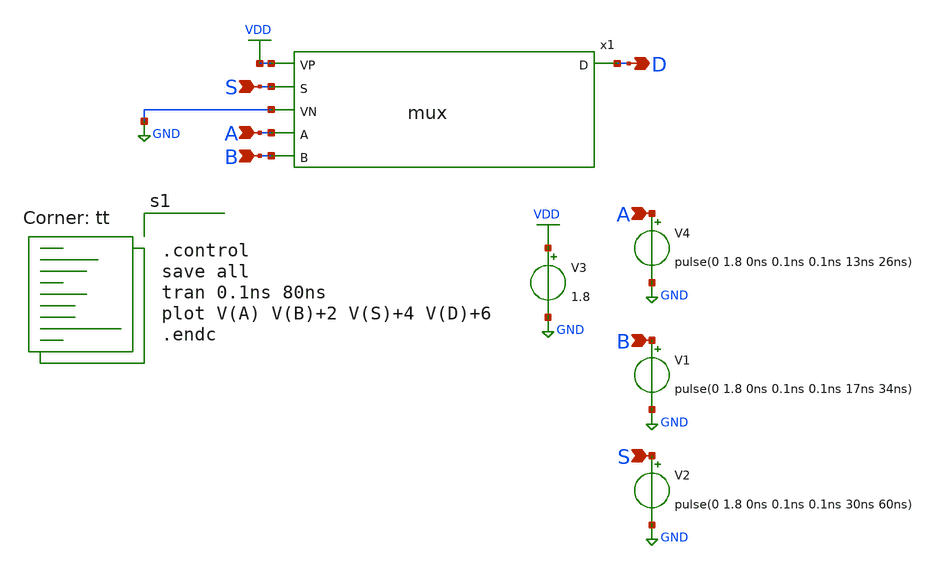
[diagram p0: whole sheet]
** sch_path: mux/xschem/tb_xschem_mux.sch
**.subckt tb_xschem_mux A B A B D S S
*.ipin A
*.ipin B
*.ipin A
*.ipin B
*.opin D
*.ipin S
*.ipin S
V3 VDD GND 1.8
V4 A GND pulse(0 1.8 0ns 0.1ns 0.1ns 13ns 26ns)
V1 B GND pulse(0 1.8 0ns 0.1ns 0.1ns 17ns 34ns)
V2 S GND pulse(0 1.8 0ns 0.1ns 0.1ns 30ns 60ns)
x1 VDD D S GND A B mux
**** begin user architecture code
.lib $::SKYWATER_MODELS/sky130.lib.spice tt


.control
save all
tran 0.1ns 80ns
plot V(A) V(B)+2 V(S)+4 V(D)+6
.endc


**** end user architecture code
**.ends

* expanding   symbol:  mux.sym # of pins=6
** sym_path: mux/xschem/mux.sym
** sch_path: mux/xschem/mux.sch
.subckt mux VP D S VN A B
*.ipin VP
*.ipin VN
*.ipin S
*.ipin A
*.ipin B
*.opin D
x1 VP net2 A net1 VN and
x2 VP net3 S B VN and
x3 VP D net3 net2 VN or
x4 VP S net1 VN inverter
.ends


* expanding   symbol:  /foss/designs/APIC_Mux_DFF/basic_cell/and/xschem/and.sym # of pins=5
** sym_path: basic_cell/and/xschem/and.sym
** sch_path: basic_cell/and/xschem/and.sch
.subckt and VP OUT B A VN
*.ipin VP
*.ipin B
*.ipin A
*.ipin VN
*.opin OUT
x1 VP net1 B A VN nand
x2 VP net1 OUT VN inverter
.ends


* expanding   symbol:  /foss/designs/APIC_Mux_DFF/basic_cell/or/xschem/or.sym # of pins=5
** sym_path: basic_cell/or/xschem/or.sym
** sch_path: basic_cell/or/xschem/or.sch
.subckt or VP OUT A B VN
*.ipin VP
*.ipin A
*.ipin B
*.ipin VN
*.opin OUT
x1 VP A B net1 VN nor
x2 VP net1 OUT VN inverter
.ends


* expanding   symbol:  /foss/designs/APIC_Mux_DFF/basic_cell/single_cell/inverter/inverter.sym # of
*+ pins=4
** sym_path: basic_cell/single_cell/inverter/inverter.sym
** sch_path: basic_cell/single_cell/inverter/inverter.sch
.subckt inverter VP A OUT VN
*.ipin A
*.ipin VP
*.ipin VN
*.opin OUT
XM1 OUT A VP VP sky130_fd_pr__pfet_01v8 L=0.15 W=3 nf=1 ad='int((nf+1)/2) * W/nf * 0.29' as='int((nf+2)/2) * W/nf * 0.29'
+ pd='2*int((nf+1)/2) * (W/nf + 0.29)' ps='2*int((nf+2)/2) * (W/nf + 0.29)' nrd='0.29 / W' nrs='0.29 / W'
+ sa=0 sb=0 sd=0 mult=1 m=1
XM2 OUT A VN VN sky130_fd_pr__nfet_01v8 L=0.15 W=1 nf=1 ad='int((nf+1)/2) * W/nf * 0.29' as='int((nf+2)/2) * W/nf * 0.29'
+ pd='2*int((nf+1)/2) * (W/nf + 0.29)' ps='2*int((nf+2)/2) * (W/nf + 0.29)' nrd='0.29 / W' nrs='0.29 / W'
+ sa=0 sb=0 sd=0 mult=1 m=1
.ends


* expanding   symbol:  /foss/designs/APIC_Mux_DFF/basic_cell/single_cell/nand/nand.sym # of pins=5
** sym_path: basic_cell/single_cell/nand/nand.sym
** sch_path: basic_cell/single_cell/nand/nand.sch
.subckt nand VP OUT B A VN
*.opin OUT
*.ipin A
*.ipin B
*.ipin VN
*.ipin VP
XM4 OUT A net1 VN sky130_fd_pr__nfet_01v8 L=0.15 W=1 nf=1 ad='int((nf+1)/2) * W/nf * 0.29' as='int((nf+2)/2) * W/nf * 0.29'
+ pd='2*int((nf+1)/2) * (W/nf + 0.29)' ps='2*int((nf+2)/2) * (W/nf + 0.29)' nrd='0.29 / W' nrs='0.29 / W'
+ sa=0 sb=0 sd=0 mult=1 m=1
XM3 net1 B VN VN sky130_fd_pr__nfet_01v8 L=0.15 W=1 nf=1 ad='int((nf+1)/2) * W/nf * 0.29' as='int((nf+2)/2) * W/nf * 0.29'
+ pd='2*int((nf+1)/2) * (W/nf + 0.29)' ps='2*int((nf+2)/2) * (W/nf + 0.29)' nrd='0.29 / W' nrs='0.29 / W'
+ sa=0 sb=0 sd=0 mult=1 m=1
XM1 OUT A VP VP sky130_fd_pr__pfet_01v8 L=0.15 W=3 nf=1 ad='int((nf+1)/2) * W/nf * 0.29' as='int((nf+2)/2) * W/nf * 0.29'
+ pd='2*int((nf+1)/2) * (W/nf + 0.29)' ps='2*int((nf+2)/2) * (W/nf + 0.29)' nrd='0.29 / W' nrs='0.29 / W'
+ sa=0 sb=0 sd=0 mult=1 m=1
XM2 OUT B VP VP sky130_fd_pr__pfet_01v8 L=0.15 W=3 nf=1 ad='int((nf+1)/2) * W/nf * 0.29' as='int((nf+2)/2) * W/nf * 0.29'
+ pd='2*int((nf+1)/2) * (W/nf + 0.29)' ps='2*int((nf+2)/2) * (W/nf + 0.29)' nrd='0.29 / W' nrs='0.29 / W'
+ sa=0 sb=0 sd=0 mult=1 m=1
.ends


* expanding   symbol:  /foss/designs/APIC_Mux_DFF/basic_cell/single_cell/nor/nor.sym # of pins=5
** sym_path: basic_cell/single_cell/nor/nor.sym
** sch_path: basic_cell/single_cell/nor/nor.sch
.subckt nor VP A B OUT VN
*.ipin A
*.ipin B
*.ipin VP
*.ipin VN
*.opin OUT
XM1 OUT A VN VN sky130_fd_pr__nfet_01v8 L=0.15 W=1 nf=1 ad='int((nf+1)/2) * W/nf * 0.29' as='int((nf+2)/2) * W/nf * 0.29'
+ pd='2*int((nf+1)/2) * (W/nf + 0.29)' ps='2*int((nf+2)/2) * (W/nf + 0.29)' nrd='0.29 / W' nrs='0.29 / W'
+ sa=0 sb=0 sd=0 mult=1 m=1
XM2 OUT B VN VN sky130_fd_pr__nfet_01v8 L=0.15 W=1 nf=1 ad='int((nf+1)/2) * W/nf * 0.29' as='int((nf+2)/2) * W/nf * 0.29'
+ pd='2*int((nf+1)/2) * (W/nf + 0.29)' ps='2*int((nf+2)/2) * (W/nf + 0.29)' nrd='0.29 / W' nrs='0.29 / W'
+ sa=0 sb=0 sd=0 mult=1 m=1
XM3 OUT B net1 VP sky130_fd_pr__pfet_01v8 L=0.15 W=3 nf=1 ad='int((nf+1)/2) * W/nf * 0.29' as='int((nf+2)/2) * W/nf * 0.29'
+ pd='2*int((nf+1)/2) * (W/nf + 0.29)' ps='2*int((nf+2)/2) * (W/nf + 0.29)' nrd='0.29 / W' nrs='0.29 / W'
+ sa=0 sb=0 sd=0 mult=1 m=1
XM4 net1 A VP VP sky130_fd_pr__pfet_01v8 L=0.15 W=3 nf=1 ad='int((nf+1)/2) * W/nf * 0.29' as='int((nf+2)/2) * W/nf * 0.29'
+ pd='2*int((nf+1)/2) * (W/nf + 0.29)' ps='2*int((nf+2)/2) * (W/nf + 0.29)' nrd='0.29 / W' nrs='0.29 / W'
+ sa=0 sb=0 sd=0 mult=1 m=1
.ends

.GLOBAL VDD
.GLOBAL GND
.end
